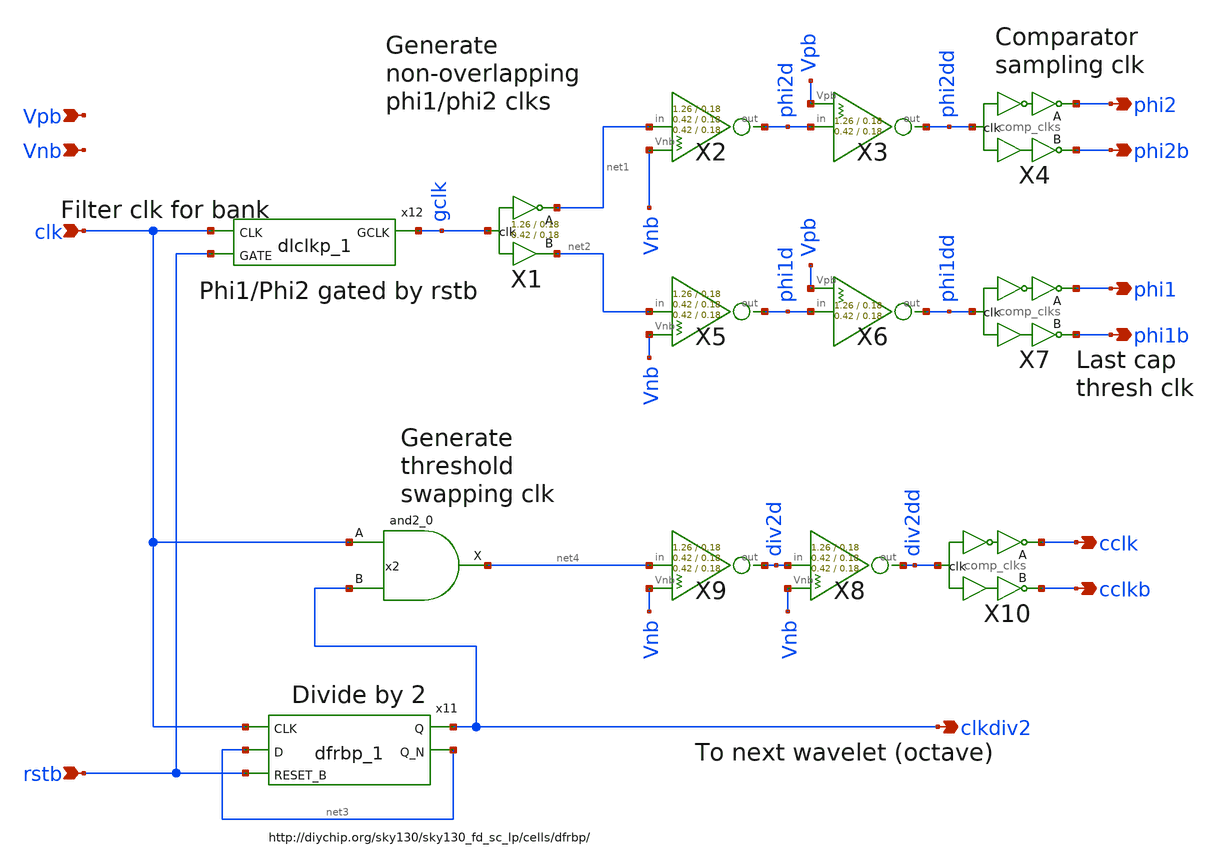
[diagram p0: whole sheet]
** sch_path: xschem/clkgen/filter_clkgen.sch
**.subckt filter_clkgen clk rstb phi2 phi2b phi1 phi1b cclk cclkb clkdiv2 Vpb Vnb
*.ipin clk
*.ipin rstb
*.opin phi2
*.opin phi2b
*.opin phi1
*.opin phi1b
*.opin cclk
*.opin cclkb
*.opin clkdiv2
*.ipin Vpb
*.ipin Vnb
X3 phi2d phi2dd Vpb inv_weak_pullup Wpmos=1.26 Lpmos=0.18 Wnmos=0.42 Lnmos=0.18
X2 net1 phi2d Vnb inv_weak_pulldown Wpmos=1.26 Lpmos=0.18 Wnmos=0.42 Lnmos=0.18
x11 clk net3 rstb gnd gnd vdd vdd clkdiv2 net3 sky130_fd_sc_lp__dfrbp_1
X4 phi2dd phi2 phi2b comp_clks Wpmos=1.26 Lpmos=0.18 Wnmos=0.42 Lnmos=0.18
X7 phi1dd phi1 phi1b comp_clks Wpmos=1.26 Lpmos=0.18 Wnmos=0.42 Lnmos=0.18
X10 div2dd cclk cclkb comp_clks Wpmos=1.26 Lpmos=0.18 Wnmos=0.42 Lnmos=0.18
X5 net2 phi1d Vnb inv_weak_pulldown Wpmos=1.26 Lpmos=0.18 Wnmos=0.42 Lnmos=0.18
X6 phi1d phi1dd Vpb inv_weak_pullup Wpmos=1.26 Lpmos=0.18 Wnmos=0.42 Lnmos=0.18
X9 net4 div2d Vnb inv_weak_pulldown Wpmos=1.26 Lpmos=0.18 Wnmos=0.42 Lnmos=0.18
X8 div2d div2dd Vnb inv_weak_pulldown Wpmos=1.26 Lpmos=0.18 Wnmos=0.42 Lnmos=0.18
x12 clk rstb gnd gnd vdd vdd gclk sky130_fd_sc_lp__dlclkp_1
X1 gclk net1 net2 comp_clks_1stage Wpmos=1.26 Lpmos=0.18 Wnmos=0.42 Lnmos=0.18
x2 clk clkdiv2 gnd gnd vdd vdd net4 sky130_fd_sc_lp__and2_0
**.ends
.end
